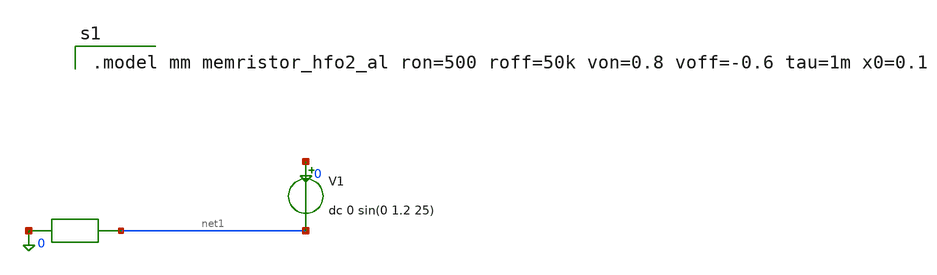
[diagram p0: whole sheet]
** sch_path: libraries/openmemristorpdk_pr/memristor_hfo2_al.sch
**.subckt memristor_hfo2_al
n1 0 net1 mm
V1 0 net1 dc 0 sin(0 1.2 25)
**** begin user architecture code

.model mm memristor_hfo2_al ron=500 roff=50k von=0.8 voff=-0.6 tau=1m x0=0.1

**** end user architecture code
**.ends
.end
